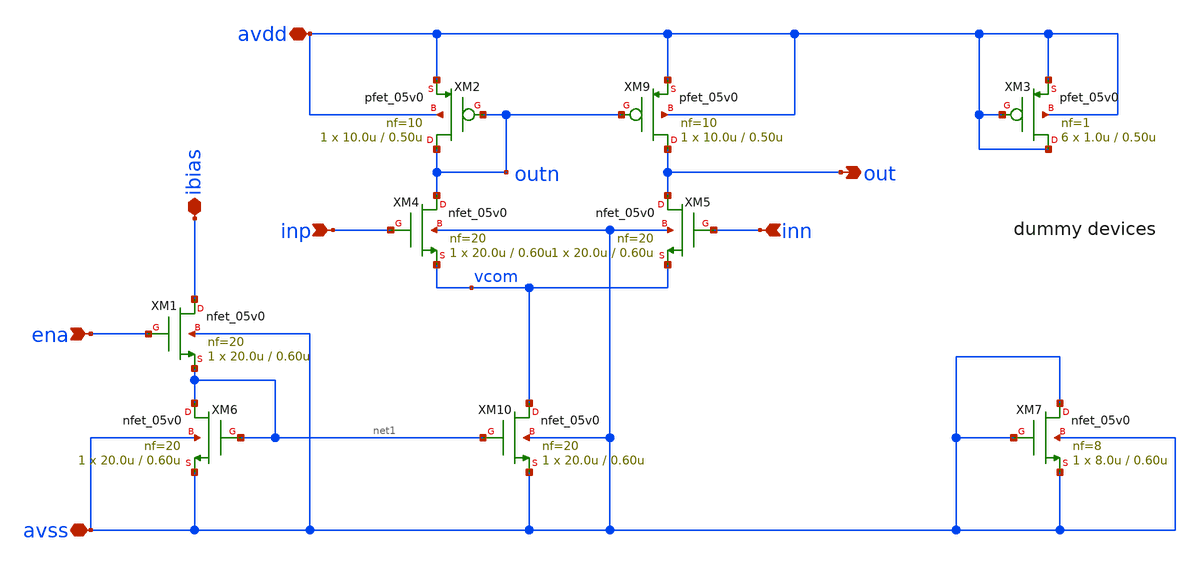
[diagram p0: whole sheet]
** sch_path: xschem/n_amp_large.sch
**.subckt n_amp_large inp inn out avdd avss ena ibias
*.ipin inp
*.ipin inn
*.opin out
*.iopin avdd
*.iopin avss
*.ipin ena
*.iopin ibias
XM9 out outn avdd avdd pfet_05v0 L=0.50u W=10.0u nf=10 ad='int((nf+1)/2) * W/nf * 0.18u' as='int((nf+2)/2) * W/nf * 0.18u'
+ pd='2*int((nf+1)/2) * (W/nf + 0.18u)' ps='2*int((nf+2)/2) * (W/nf + 0.18u)' nrd='0.18u / W' nrs='0.18u / W'
+ sa=0 sb=0 sd=0 m=1 par=1
XM10 vcom net1 avss avss nfet_05v0 L=0.60u W=20.0u nf=20 ad='int((nf+1)/2) * W/nf * 0.18u' as='int((nf+2)/2) * W/nf * 0.18u'
+ pd='2*int((nf+1)/2) * (W/nf + 0.18u)' ps='2*int((nf+2)/2) * (W/nf + 0.18u)' nrd='0.18u / W' nrs='0.18u / W'
+ sa=0 sb=0 sd=0 m=1
XM1 ibias ena net1 avss nfet_05v0 L=0.60u W=20.0u nf=20 ad='int((nf+1)/2) * W/nf * 0.18u' as='int((nf+2)/2) * W/nf * 0.18u'
+ pd='2*int((nf+1)/2) * (W/nf + 0.18u)' ps='2*int((nf+2)/2) * (W/nf + 0.18u)' nrd='0.18u / W' nrs='0.18u / W'
+ sa=0 sb=0 sd=0 m=1
XM6 net1 net1 avss avss nfet_05v0 L=0.60u W=20.0u nf=20 ad='int((nf+1)/2) * W/nf * 0.18u' as='int((nf+2)/2) * W/nf * 0.18u'
+ pd='2*int((nf+1)/2) * (W/nf + 0.18u)' ps='2*int((nf+2)/2) * (W/nf + 0.18u)' nrd='0.18u / W' nrs='0.18u / W'
+ sa=0 sb=0 sd=0 m=1
XM4 outn inp vcom avss nfet_05v0 L=0.60u W=20.0u nf=20 ad='int((nf+1)/2) * W/nf * 0.18u' as='int((nf+2)/2) * W/nf * 0.18u'
+ pd='2*int((nf+1)/2) * (W/nf + 0.18u)' ps='2*int((nf+2)/2) * (W/nf + 0.18u)' nrd='0.18u / W' nrs='0.18u / W'
+ sa=0 sb=0 sd=0 m=1
XM5 out inn vcom avss nfet_05v0 L=0.60u W=20.0u nf=20 ad='int((nf+1)/2) * W/nf * 0.18u' as='int((nf+2)/2) * W/nf * 0.18u'
+ pd='2*int((nf+1)/2) * (W/nf + 0.18u)' ps='2*int((nf+2)/2) * (W/nf + 0.18u)' nrd='0.18u / W' nrs='0.18u / W'
+ sa=0 sb=0 sd=0 m=1
XM2 outn outn avdd avdd pfet_05v0 L=0.50u W=10.0u nf=10 ad='int((nf+1)/2) * W/nf * 0.18u' as='int((nf+2)/2) * W/nf * 0.18u'
+ pd='2*int((nf+1)/2) * (W/nf + 0.18u)' ps='2*int((nf+2)/2) * (W/nf + 0.18u)' nrd='0.18u / W' nrs='0.18u / W'
+ sa=0 sb=0 sd=0 m=1 par=1
XM3 avdd avdd avdd avdd pfet_05v0 L=0.50u W=1.0u nf=1 ad='int((nf+1)/2) * W/nf * 0.18u' as='int((nf+2)/2) * W/nf * 0.18u'
+ pd='2*int((nf+1)/2) * (W/nf + 0.18u)' ps='2*int((nf+2)/2) * (W/nf + 0.18u)' nrd='0.18u / W' nrs='0.18u / W'
+ sa=0 sb=0 sd=0 m=6 par=6
XM7 avss avss avss avss nfet_05v0 L=0.60u W=8.0u nf=8 ad='int((nf+1)/2) * W/nf * 0.18u' as='int((nf+2)/2) * W/nf * 0.18u'
+ pd='2*int((nf+1)/2) * (W/nf + 0.18u)' ps='2*int((nf+2)/2) * (W/nf + 0.18u)' nrd='0.18u / W' nrs='0.18u / W'
+ sa=0 sb=0 sd=0 m=1
**.ends
.end
